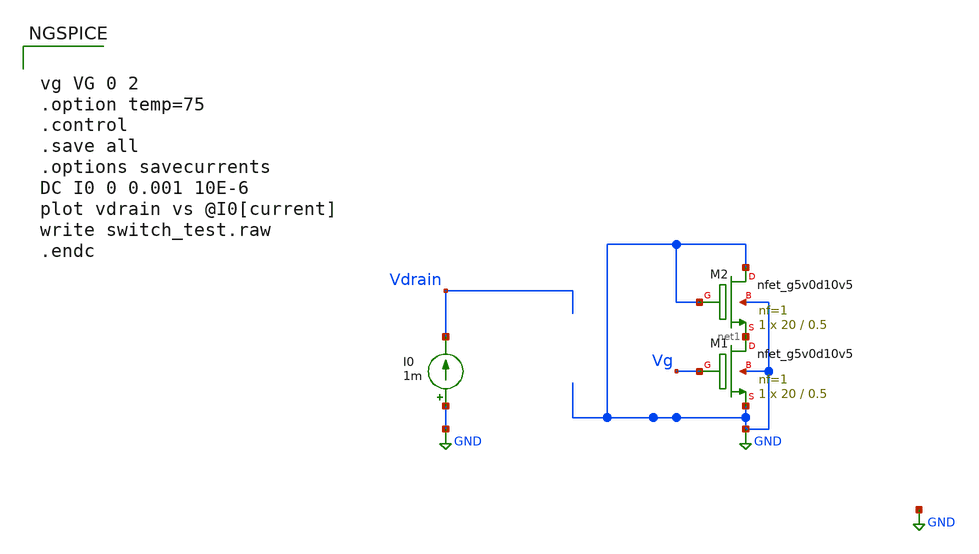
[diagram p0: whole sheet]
** sch_path: design/system/vcomp_limit_test.sch
**.subckt vcomp_limit_test
XM1 net1 Vg GND GND sky130_fd_pr__nfet_g5v0d10v5 L=0.5 W=20 nf=1 ad='int((nf+1)/2) * W/nf * 0.29' as='int((nf+2)/2) * W/nf * 0.29'
+ pd='2*int((nf+1)/2) * (W/nf + 0.29)' ps='2*int((nf+2)/2) * (W/nf + 0.29)' nrd='0.29 / W' nrs='0.29 / W'
+ sa=0 sb=0 sd=0 mult=1 m=1
I0 GND Vdrain 1m
XM2 GND GND net1 GND sky130_fd_pr__nfet_g5v0d10v5 L=0.5 W=20 nf=1 ad='int((nf+1)/2) * W/nf * 0.29' as='int((nf+2)/2) * W/nf * 0.29'
+ pd='2*int((nf+1)/2) * (W/nf + 0.29)' ps='2*int((nf+2)/2) * (W/nf + 0.29)' nrd='0.29 / W' nrs='0.29 / W'
+ sa=0 sb=0 sd=0 mult=1 m=1
**** begin user architecture code


vg VG 0 2
.option temp=75
.control
.save all
.options savecurrents
DC I0 0 0.001 10E-6
plot vdrain vs @I0[current]
write switch_test.raw
.endc



.include $::SKYWATER_MODELS/cells/nfet_01v8/sky130_fd_pr__nfet_01v8__tt.corner.spice
.include $::SKYWATER_MODELS/cells/nfet_01v8_lvt/sky130_fd_pr__nfet_01v8_lvt__tt.corner.spice
.include $::SKYWATER_MODELS/cells/pfet_01v8/sky130_fd_pr__pfet_01v8__tt.corner.spice
.include $::SKYWATER_MODELS/cells/nfet_03v3_nvt/sky130_fd_pr__nfet_03v3_nvt__tt.corner.spice
.include $::SKYWATER_MODELS/cells/nfet_05v0_nvt/sky130_fd_pr__nfet_05v0_nvt__tt.corner.spice
.include $::SKYWATER_MODELS/cells/esd_nfet_01v8/sky130_fd_pr__esd_nfet_01v8__tt.corner.spice
.include $::SKYWATER_MODELS/cells/pfet_01v8_lvt/sky130_fd_pr__pfet_01v8_lvt__tt.corner.spice
.include $::SKYWATER_MODELS/cells/pfet_01v8_hvt/sky130_fd_pr__pfet_01v8_hvt__tt.corner.spice
.include $::SKYWATER_MODELS/cells/esd_pfet_g5v0d10v5/sky130_fd_pr__esd_pfet_g5v0d10v5__tt.corner.spice
.include $::SKYWATER_MODELS/cells/pfet_g5v0d10v5/sky130_fd_pr__pfet_g5v0d10v5__tt.corner.spice
.include $::SKYWATER_MODELS/cells/pfet_g5v0d16v0/sky130_fd_pr__pfet_g5v0d16v0__tt.corner.spice
.include $::SKYWATER_MODELS/cells/nfet_g5v0d10v5/sky130_fd_pr__nfet_g5v0d10v5__tt.corner.spice
.include $::SKYWATER_MODELS/cells/nfet_g5v0d16v0/sky130_fd_pr__nfet_g5v0d16v0__tt_discrete.corner.spice
.include $::SKYWATER_MODELS/cells/esd_nfet_g5v0d10v5/sky130_fd_pr__esd_nfet_g5v0d10v5__tt.corner.spice
.include $::SKYWATER_MODELS/models/corners/tt/nonfet.spice
* Mismatch parameters
.include $::SKYWATER_MODELS/cells/nfet_01v8/sky130_fd_pr__nfet_01v8__mismatch.corner.spice
.include $::SKYWATER_MODELS/cells/pfet_01v8/sky130_fd_pr__pfet_01v8__mismatch.corner.spice
.include $::SKYWATER_MODELS/cells/nfet_01v8_lvt/sky130_fd_pr__nfet_01v8_lvt__mismatch.corner.spice
.include $::SKYWATER_MODELS/cells/pfet_01v8_lvt/sky130_fd_pr__pfet_01v8_lvt__mismatch.corner.spice
.include $::SKYWATER_MODELS/cells/pfet_01v8_hvt/sky130_fd_pr__pfet_01v8_hvt__mismatch.corner.spice
.include $::SKYWATER_MODELS/cells/nfet_g5v0d10v5/sky130_fd_pr__nfet_g5v0d10v5__mismatch.corner.spice
.include $::SKYWATER_MODELS/cells/pfet_g5v0d10v5/sky130_fd_pr__pfet_g5v0d10v5__mismatch.corner.spice
.include $::SKYWATER_MODELS/cells/nfet_05v0_nvt/sky130_fd_pr__nfet_05v0_nvt__mismatch.corner.spice
.include $::SKYWATER_MODELS/cells/nfet_03v3_nvt/sky130_fd_pr__nfet_03v3_nvt__mismatch.corner.spice
* Resistor$::SKYWATER_MODELS/Capacitor
.include $::SKYWATER_MODELS/models/r+c/res_typical__cap_typical.spice
.include $::SKYWATER_MODELS/models/r+c/res_typical__cap_typical__lin.spice
* Special cells
.include $::SKYWATER_MODELS/models/corners/tt/specialized_cells.spice
* All models
.include $::SKYWATER_MODELS/models/all.spice
* Corner
.include $::SKYWATER_MODELS/models/corners/tt/rf.spice

**** end user architecture code
**.ends
.GLOBAL GND
.end
